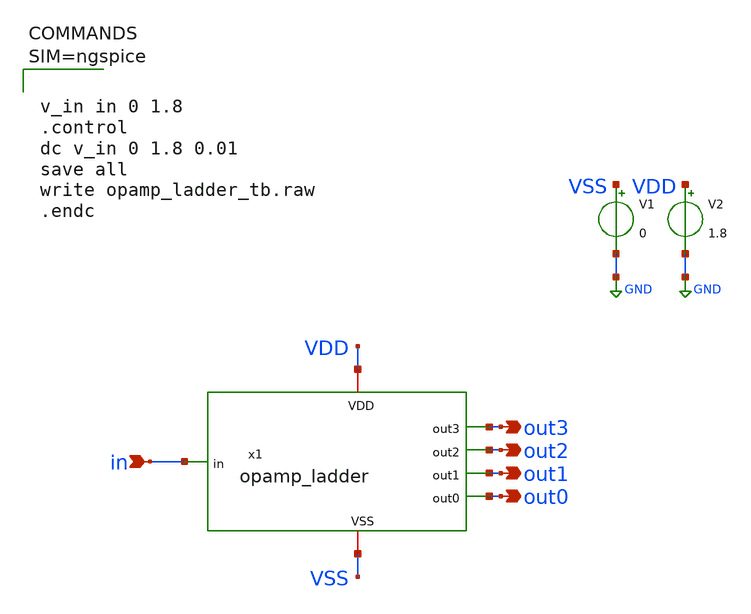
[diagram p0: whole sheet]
** sch_path: xschem/opamp_ladder_tb.sch
**.subckt opamp_ladder_tb out0 out1 out2 out3 in
*.opin out0
*.opin out1
*.opin out2
*.opin out3
*.ipin in
x1 VDD in VSS out3 out2 out1 out0 opamp_ladder
V1 VSS GND 0
V2 VDD GND 1.8
**** begin user architecture code

** opencircuitdesign pdks install
.lib $::SKYWATER_MODELS/sky130.lib.spice tt





v_in in 0 1.8
.control
dc v_in 0 1.8 0.01
save all
write opamp_ladder_tb.raw
.endc



**** end user architecture code
**.ends

* expanding   symbol:  opamp_ladder.sym # of pins=7
** sym_path: xschem/opamp_ladder.sym
** sch_path: xschem/opamp_ladder.sch
.subckt opamp_ladder VDD in VSS out3 out2 out1 out0
*.opin out0
*.opin out2
*.opin out3
*.ipin in
*.iopin VDD
*.iopin VSS
*.opin out1
x1 VDD VSS net4 in out0 VSS opamp
XR2 VSS net4 VSS sky130_fd_pr__res_generic_nd W=1 L=8.4 mult=1 m=1
XR3 net4 net3 VSS sky130_fd_pr__res_generic_nd W=1 L=8.4 mult=1 m=1
XR4 net3 net2 VSS sky130_fd_pr__res_generic_nd W=1 L=8.4 mult=1 m=1
XR5 net2 net1 VSS sky130_fd_pr__res_generic_nd W=1 L=8.4 mult=1 m=1
x2 VDD VSS net3 in out1 VSS opamp
x3 VDD VSS net2 in out2 VSS opamp
x4 VDD VSS net1 in out3 VSS opamp
XR1 net1 VDD VSS sky130_fd_pr__res_generic_nd W=1 L=8.4 mult=1 m=1
.ends


* expanding   symbol:  opamp.sym # of pins=6
** sym_path: xschem/opamp.sym
** sch_path: xschem/opamp.sch
.subckt opamp VDD ZREF vin_n vin_p Vout VGND
*.ipin vin_n
*.ipin vin_p
*.opin Vout
*.iopin VDD
*.iopin ZREF
*.iopin VGND
XM1 net1 vin_n net3 net3 sky130_fd_pr__pfet_01v8 L=0.6 W=6 nf=1 ad='W * 0.29' as='W * 0.29' pd='2 * (W + 0.29)'
+ ps='2 * (W + 0.29)' nrd='0.29 / W' nrs='0.29 / W' sa=0 sb=0 sd=0 mult=1 m=1
XM2 net2 vin_p net3 net3 sky130_fd_pr__pfet_01v8 L=0.6 W=6 nf=1 ad='W * 0.29' as='W * 0.29' pd='2 * (W + 0.29)'
+ ps='2 * (W + 0.29)' nrd='0.29 / W' nrs='0.29 / W' sa=0 sb=0 sd=0 mult=1 m=1
XM3 net1 net1 VGND VGND sky130_fd_pr__nfet_01v8 L=0.6 W=6 nf=1 ad='W * 0.29' as='W * 0.29' pd='2 * (W + 0.29)'
+ ps='2 * (W + 0.29)' nrd='0.29 / W' nrs='0.29 / W' sa=0 sb=0 sd=0 mult=1 m=1
XM4 net2 net1 VGND VGND sky130_fd_pr__nfet_01v8 L=0.6 W=6 nf=1 ad='W * 0.29' as='W * 0.29' pd='2 * (W + 0.29)'
+ ps='2 * (W + 0.29)' nrd='0.29 / W' nrs='0.29 / W' sa=0 sb=0 sd=0 mult=1 m=1
XM5 net3 VGND VDD VDD sky130_fd_pr__pfet_01v8 L=0.6 W=6 nf=1 ad='W * 0.29' as='W * 0.29' pd='2 * (W + 0.29)'
+ ps='2 * (W + 0.29)' nrd='0.29 / W' nrs='0.29 / W' sa=0 sb=0 sd=0 mult=1 m=1
XM7 Vout VGND VDD VDD sky130_fd_pr__pfet_01v8 L=0.6 W=6 nf=1 ad='W * 0.29' as='W * 0.29' pd='2 * (W + 0.29)'
+ ps='2 * (W + 0.29)' nrd='0.29 / W' nrs='0.29 / W' sa=0 sb=0 sd=0 mult=1 m=1
XM8 ZREF VGND VDD VDD sky130_fd_pr__pfet_01v8 L=0.6 W=6 nf=1 ad='W * 0.29' as='W * 0.29' pd='2 * (W + 0.29)'
+ ps='2 * (W + 0.29)' nrd='0.29 / W' nrs='0.29 / W' sa=0 sb=0 sd=0 mult=1 m=1
XM9 net4 VDD net2 VGND sky130_fd_pr__nfet_01v8 L=0.6 W=1 nf=1 ad='W * 0.29' as='W * 0.29' pd='2 * (W + 0.29)'
+ ps='2 * (W + 0.29)' nrd='0.29 / W' nrs='0.29 / W' sa=0 sb=0 sd=0 mult=1 m=1
XC1 net4 Vout sky130_fd_pr__cap_mim_m3_1 W=17.55 L=15 MF=1 m=1
XM6 Vout net2 VGND VGND sky130_fd_pr__nfet_01v8 L=0.6 W=6 nf=1 ad='W * 0.29' as='W * 0.29' pd='2 * (W + 0.29)'
+ ps='2 * (W + 0.29)' nrd='0.29 / W' nrs='0.29 / W' sa=0 sb=0 sd=0 mult=1 m=1
XR1 ZREF VDD VGND sky130_fd_pr__res_generic_nd W=1 L=5 mult=1 m=1
XR2 VGND ZREF VGND sky130_fd_pr__res_generic_nd W=1 L=5 mult=1 m=1
.ends

.GLOBAL GND
.end
